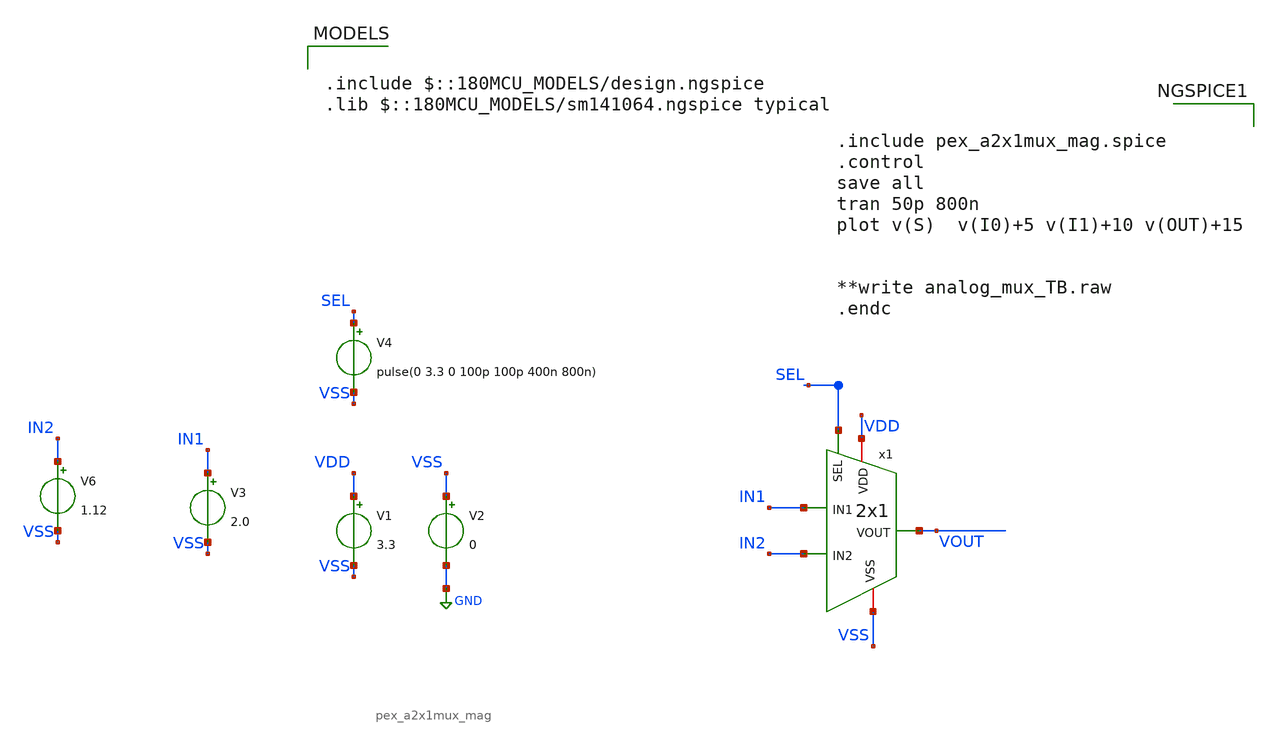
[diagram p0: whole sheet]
** sch_path: Clock_Generator_PAKISTAN_02/Schematics/pex_analog_mux_test.sch
**.subckt pex_analog_mux_test
V1 VDD VSS 3.3
V2 VSS GND 0
V4 SEL VSS pulse(0 3.3 0 100p 100p 400n 800n)
V6 IN2 VSS 1.12
V3 IN1 VSS 2.0
x1 IN1 VDD VOUT SEL VSS IN2 pex_a2x1mux_mag
**** begin user architecture code


.include pex_a2x1mux_mag.spice
.control
save all
tran 50p 800n
plot v(S)  v(I0)+5 v(I1)+10 v(OUT)+15


**write analog_mux_TB.raw
.endc



.include $::180MCU_MODELS/design.ngspice
.lib $::180MCU_MODELS/sm141064.ngspice typical

**** end user architecture code
**.ends
.GLOBAL GND
.end
